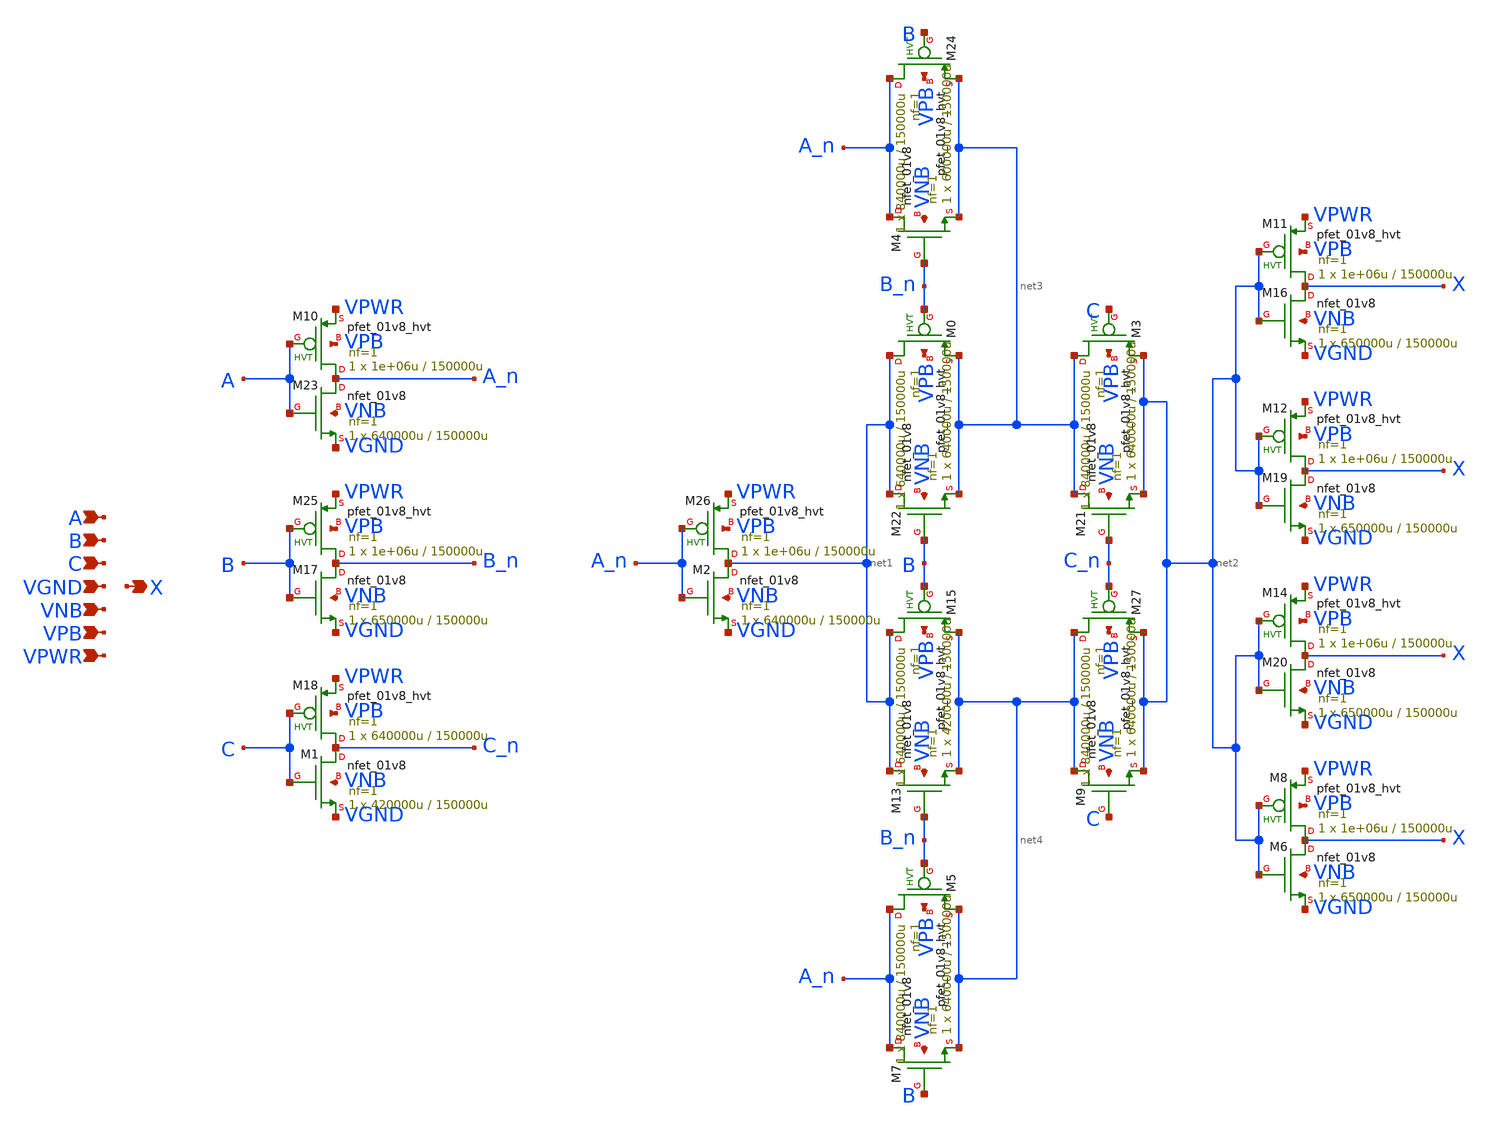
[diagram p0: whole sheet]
** sch_path: schematics/xor3/sky130_fd_sc_hd__xor3_4.sch
**.subckt sky130_fd_sc_hd__xor3_4 A B C VGND VNB VPB VPWR X
*.ipin A
*.ipin B
*.ipin C
*.ipin VGND
*.ipin VNB
*.ipin VPB
*.ipin VPWR
*.opin X
XM10 A_n A VPWR VPB sky130_fd_pr__pfet_01v8_hvt L=150000u W=1e+06u nf=1 ad='int((1 + 1)/2) * 1e+06u / 1 * 0.29'
+ as='int((1 + 2)/2) * 1e+06u / 1 * 0.29' pd='2*int((1 + 1)/2) * (1e+06u / 1 + 0.29)' ps='2*int((1 + 2)/2) * (1e+06u / 1 + 0.29)'
+ nrd='0.29 / 1e+06u ' nrs='0.29 / 1e+06u ' sa=0 sb=0 sd=0 mult=1 m=1
XM23 A_n A VGND VNB sky130_fd_pr__nfet_01v8 L=150000u W=640000u nf=1 ad='int((1 + 1)/2) * 640000u / 1 * 0.29'
+ as='int((1 + 2)/2) * 640000u / 1 * 0.29' pd='2*int((1 + 1)/2) * (640000u / 1 + 0.29)' ps='2*int((1 + 2)/2) * (640000u / 1 + 0.29)'
+ nrd='0.29 / 640000u ' nrs='0.29 / 640000u ' sa=0 sb=0 sd=0 mult=1 m=1
XM26 net1 A_n VPWR VPB sky130_fd_pr__pfet_01v8_hvt L=150000u W=1e+06u nf=1 ad='int((1 + 1)/2) * 1e+06u / 1 * 0.29'
+ as='int((1 + 2)/2) * 1e+06u / 1 * 0.29' pd='2*int((1 + 1)/2) * (1e+06u / 1 + 0.29)' ps='2*int((1 + 2)/2) * (1e+06u / 1 + 0.29)'
+ nrd='0.29 / 1e+06u ' nrs='0.29 / 1e+06u ' sa=0 sb=0 sd=0 mult=1 m=1
XM2 net1 A_n VGND VNB sky130_fd_pr__nfet_01v8 L=150000u W=640000u nf=1 ad='int((1 + 1)/2) * 640000u / 1 * 0.29'
+ as='int((1 + 2)/2) * 640000u / 1 * 0.29' pd='2*int((1 + 1)/2) * (640000u / 1 + 0.29)' ps='2*int((1 + 2)/2) * (640000u / 1 + 0.29)'
+ nrd='0.29 / 640000u ' nrs='0.29 / 640000u ' sa=0 sb=0 sd=0 mult=1 m=1
XM8 X net2 VPWR VPB sky130_fd_pr__pfet_01v8_hvt L=150000u W=1e+06u nf=1 ad='int((1 + 1)/2) * 1e+06u / 1 * 0.29'
+ as='int((1 + 2)/2) * 1e+06u / 1 * 0.29' pd='2*int((1 + 1)/2) * (1e+06u / 1 + 0.29)' ps='2*int((1 + 2)/2) * (1e+06u / 1 + 0.29)'
+ nrd='0.29 / 1e+06u ' nrs='0.29 / 1e+06u ' sa=0 sb=0 sd=0 mult=1 m=1
XM6 X net2 VGND VNB sky130_fd_pr__nfet_01v8 L=150000u W=650000u nf=1 ad='int((1 + 1)/2) * 650000u / 1 * 0.29'
+ as='int((1 + 2)/2) * 650000u / 1 * 0.29' pd='2*int((1 + 1)/2) * (650000u / 1 + 0.29)' ps='2*int((1 + 2)/2) * (650000u / 1 + 0.29)'
+ nrd='0.29 / 650000u ' nrs='0.29 / 650000u ' sa=0 sb=0 sd=0 mult=1 m=1
XM11 X net2 VPWR VPB sky130_fd_pr__pfet_01v8_hvt L=150000u W=1e+06u nf=1 ad='int((1 + 1)/2) * 1e+06u / 1 * 0.29'
+ as='int((1 + 2)/2) * 1e+06u / 1 * 0.29' pd='2*int((1 + 1)/2) * (1e+06u / 1 + 0.29)' ps='2*int((1 + 2)/2) * (1e+06u / 1 + 0.29)'
+ nrd='0.29 / 1e+06u ' nrs='0.29 / 1e+06u ' sa=0 sb=0 sd=0 mult=1 m=1
XM16 X net2 VGND VNB sky130_fd_pr__nfet_01v8 L=150000u W=650000u nf=1 ad='int((1 + 1)/2) * 650000u / 1 * 0.29'
+ as='int((1 + 2)/2) * 650000u / 1 * 0.29' pd='2*int((1 + 1)/2) * (650000u / 1 + 0.29)' ps='2*int((1 + 2)/2) * (650000u / 1 + 0.29)'
+ nrd='0.29 / 650000u ' nrs='0.29 / 650000u ' sa=0 sb=0 sd=0 mult=1 m=1
XM12 X net2 VPWR VPB sky130_fd_pr__pfet_01v8_hvt L=150000u W=1e+06u nf=1 ad='int((1 + 1)/2) * 1e+06u / 1 * 0.29'
+ as='int((1 + 2)/2) * 1e+06u / 1 * 0.29' pd='2*int((1 + 1)/2) * (1e+06u / 1 + 0.29)' ps='2*int((1 + 2)/2) * (1e+06u / 1 + 0.29)'
+ nrd='0.29 / 1e+06u ' nrs='0.29 / 1e+06u ' sa=0 sb=0 sd=0 mult=1 m=1
XM19 X net2 VGND VNB sky130_fd_pr__nfet_01v8 L=150000u W=650000u nf=1 ad='int((1 + 1)/2) * 650000u / 1 * 0.29'
+ as='int((1 + 2)/2) * 650000u / 1 * 0.29' pd='2*int((1 + 1)/2) * (650000u / 1 + 0.29)' ps='2*int((1 + 2)/2) * (650000u / 1 + 0.29)'
+ nrd='0.29 / 650000u ' nrs='0.29 / 650000u ' sa=0 sb=0 sd=0 mult=1 m=1
XM14 X net2 VPWR VPB sky130_fd_pr__pfet_01v8_hvt L=150000u W=1e+06u nf=1 ad='int((1 + 1)/2) * 1e+06u / 1 * 0.29'
+ as='int((1 + 2)/2) * 1e+06u / 1 * 0.29' pd='2*int((1 + 1)/2) * (1e+06u / 1 + 0.29)' ps='2*int((1 + 2)/2) * (1e+06u / 1 + 0.29)'
+ nrd='0.29 / 1e+06u ' nrs='0.29 / 1e+06u ' sa=0 sb=0 sd=0 mult=1 m=1
XM20 X net2 VGND VNB sky130_fd_pr__nfet_01v8 L=150000u W=650000u nf=1 ad='int((1 + 1)/2) * 650000u / 1 * 0.29'
+ as='int((1 + 2)/2) * 650000u / 1 * 0.29' pd='2*int((1 + 1)/2) * (650000u / 1 + 0.29)' ps='2*int((1 + 2)/2) * (650000u / 1 + 0.29)'
+ nrd='0.29 / 650000u ' nrs='0.29 / 650000u ' sa=0 sb=0 sd=0 mult=1 m=1
XM25 B_n B VPWR VPB sky130_fd_pr__pfet_01v8_hvt L=150000u W=1e+06u nf=1 ad='int((1 + 1)/2) * 1e+06u / 1 * 0.29'
+ as='int((1 + 2)/2) * 1e+06u / 1 * 0.29' pd='2*int((1 + 1)/2) * (1e+06u / 1 + 0.29)' ps='2*int((1 + 2)/2) * (1e+06u / 1 + 0.29)'
+ nrd='0.29 / 1e+06u ' nrs='0.29 / 1e+06u ' sa=0 sb=0 sd=0 mult=1 m=1
XM17 B_n B VGND VNB sky130_fd_pr__nfet_01v8 L=150000u W=650000u nf=1 ad='int((1 + 1)/2) * 650000u / 1 * 0.29'
+ as='int((1 + 2)/2) * 650000u / 1 * 0.29' pd='2*int((1 + 1)/2) * (650000u / 1 + 0.29)' ps='2*int((1 + 2)/2) * (650000u / 1 + 0.29)'
+ nrd='0.29 / 650000u ' nrs='0.29 / 650000u ' sa=0 sb=0 sd=0 mult=1 m=1
XM18 C_n C VPWR VPB sky130_fd_pr__pfet_01v8_hvt L=150000u W=640000u nf=1 ad='int((1 + 1)/2) * 640000u / 1 * 0.29'
+ as='int((1 + 2)/2) * 640000u / 1 * 0.29' pd='2*int((1 + 1)/2) * (640000u / 1 + 0.29)' ps='2*int((1 + 2)/2) * (640000u / 1 + 0.29)'
+ nrd='0.29 / 640000u ' nrs='0.29 / 640000u ' sa=0 sb=0 sd=0 mult=1 m=1
XM1 C_n C VGND VNB sky130_fd_pr__nfet_01v8 L=150000u W=420000u nf=1 ad='int((1 + 1)/2) * 420000u / 1 * 0.29'
+ as='int((1 + 2)/2) * 420000u / 1 * 0.29' pd='2*int((1 + 1)/2) * (420000u / 1 + 0.29)' ps='2*int((1 + 2)/2) * (420000u / 1 + 0.29)'
+ nrd='0.29 / 420000u ' nrs='0.29 / 420000u ' sa=0 sb=0 sd=0 mult=1 m=1
XM0 net1 B_n net3 VPB sky130_fd_pr__pfet_01v8_hvt L=150000u W=640000u nf=1 ad='int((1 + 1)/2) * 640000u / 1 * 0.29'
+ as='int((1 + 2)/2) * 640000u / 1 * 0.29' pd='2*int((1 + 1)/2) * (640000u / 1 + 0.29)' ps='2*int((1 + 2)/2) * (640000u / 1 + 0.29)'
+ nrd='0.29 / 640000u ' nrs='0.29 / 640000u ' sa=0 sb=0 sd=0 mult=1 m=1
XM22 net1 B net3 VNB sky130_fd_pr__nfet_01v8 L=150000u W=640000u nf=1 ad='int((1 + 1)/2) * 640000u / 1 * 0.29'
+ as='int((1 + 2)/2) * 640000u / 1 * 0.29' pd='2*int((1 + 1)/2) * (640000u / 1 + 0.29)' ps='2*int((1 + 2)/2) * (640000u / 1 + 0.29)'
+ nrd='0.29 / 640000u ' nrs='0.29 / 640000u ' sa=0 sb=0 sd=0 mult=1 m=1
XM5 A_n B_n net4 VPB sky130_fd_pr__pfet_01v8_hvt L=150000u W=840000u nf=1 ad='int((1 + 1)/2) * 840000u / 1 * 0.29'
+ as='int((1 + 2)/2) * 840000u / 1 * 0.29' pd='2*int((1 + 1)/2) * (840000u / 1 + 0.29)' ps='2*int((1 + 2)/2) * (840000u / 1 + 0.29)'
+ nrd='0.29 / 840000u ' nrs='0.29 / 840000u ' sa=0 sb=0 sd=0 mult=1 m=1
XM7 A_n B net4 VNB sky130_fd_pr__nfet_01v8 L=150000u W=640000u nf=1 ad='int((1 + 1)/2) * 640000u / 1 * 0.29'
+ as='int((1 + 2)/2) * 640000u / 1 * 0.29' pd='2*int((1 + 1)/2) * (640000u / 1 + 0.29)' ps='2*int((1 + 2)/2) * (640000u / 1 + 0.29)'
+ nrd='0.29 / 640000u ' nrs='0.29 / 640000u ' sa=0 sb=0 sd=0 mult=1 m=1
XM27 net4 C_n net2 VPB sky130_fd_pr__pfet_01v8_hvt L=150000u W=840000u nf=1 ad='int((1 + 1)/2) * 840000u / 1 * 0.29'
+ as='int((1 + 2)/2) * 840000u / 1 * 0.29' pd='2*int((1 + 1)/2) * (840000u / 1 + 0.29)' ps='2*int((1 + 2)/2) * (840000u / 1 + 0.29)'
+ nrd='0.29 / 840000u ' nrs='0.29 / 840000u ' sa=0 sb=0 sd=0 mult=1 m=1
XM9 net4 C net2 VNB sky130_fd_pr__nfet_01v8 L=150000u W=640000u nf=1 ad='int((1 + 1)/2) * 640000u / 1 * 0.29'
+ as='int((1 + 2)/2) * 640000u / 1 * 0.29' pd='2*int((1 + 1)/2) * (640000u / 1 + 0.29)' ps='2*int((1 + 2)/2) * (640000u / 1 + 0.29)'
+ nrd='0.29 / 640000u ' nrs='0.29 / 640000u ' sa=0 sb=0 sd=0 mult=1 m=1
XM15 net1 B net4 VPB sky130_fd_pr__pfet_01v8_hvt L=150000u W=640000u nf=1 ad='int((1 + 1)/2) * 640000u / 1 * 0.29'
+ as='int((1 + 2)/2) * 640000u / 1 * 0.29' pd='2*int((1 + 1)/2) * (640000u / 1 + 0.29)' ps='2*int((1 + 2)/2) * (640000u / 1 + 0.29)'
+ nrd='0.29 / 640000u ' nrs='0.29 / 640000u ' sa=0 sb=0 sd=0 mult=1 m=1
XM13 net1 B_n net4 VNB sky130_fd_pr__nfet_01v8 L=150000u W=420000u nf=1 ad='int((1 + 1)/2) * 420000u / 1 * 0.29'
+ as='int((1 + 2)/2) * 420000u / 1 * 0.29' pd='2*int((1 + 1)/2) * (420000u / 1 + 0.29)' ps='2*int((1 + 2)/2) * (420000u / 1 + 0.29)'
+ nrd='0.29 / 420000u ' nrs='0.29 / 420000u ' sa=0 sb=0 sd=0 mult=1 m=1
XM24 A_n B net3 VPB sky130_fd_pr__pfet_01v8_hvt L=150000u W=840000u nf=1 ad='int((1 + 1)/2) * 840000u / 1 * 0.29'
+ as='int((1 + 2)/2) * 840000u / 1 * 0.29' pd='2*int((1 + 1)/2) * (840000u / 1 + 0.29)' ps='2*int((1 + 2)/2) * (840000u / 1 + 0.29)'
+ nrd='0.29 / 840000u ' nrs='0.29 / 840000u ' sa=0 sb=0 sd=0 mult=1 m=1
XM4 A_n B_n net3 VNB sky130_fd_pr__nfet_01v8 L=150000u W=600000u nf=1 ad='int((1 + 1)/2) * 600000u / 1 * 0.29'
+ as='int((1 + 2)/2) * 600000u / 1 * 0.29' pd='2*int((1 + 1)/2) * (600000u / 1 + 0.29)' ps='2*int((1 + 2)/2) * (600000u / 1 + 0.29)'
+ nrd='0.29 / 600000u ' nrs='0.29 / 600000u ' sa=0 sb=0 sd=0 mult=1 m=1
XM3 net3 C net2 VPB sky130_fd_pr__pfet_01v8_hvt L=150000u W=840000u nf=1 ad='int((1 + 1)/2) * 840000u / 1 * 0.29'
+ as='int((1 + 2)/2) * 840000u / 1 * 0.29' pd='2*int((1 + 1)/2) * (840000u / 1 + 0.29)' ps='2*int((1 + 2)/2) * (840000u / 1 + 0.29)'
+ nrd='0.29 / 840000u ' nrs='0.29 / 840000u ' sa=0 sb=0 sd=0 mult=1 m=1
XM21 net3 C_n net2 VNB sky130_fd_pr__nfet_01v8 L=150000u W=640000u nf=1 ad='int((1 + 1)/2) * 640000u / 1 * 0.29'
+ as='int((1 + 2)/2) * 640000u / 1 * 0.29' pd='2*int((1 + 1)/2) * (640000u / 1 + 0.29)' ps='2*int((1 + 2)/2) * (640000u / 1 + 0.29)'
+ nrd='0.29 / 640000u ' nrs='0.29 / 640000u ' sa=0 sb=0 sd=0 mult=1 m=1
**.ends
.end
